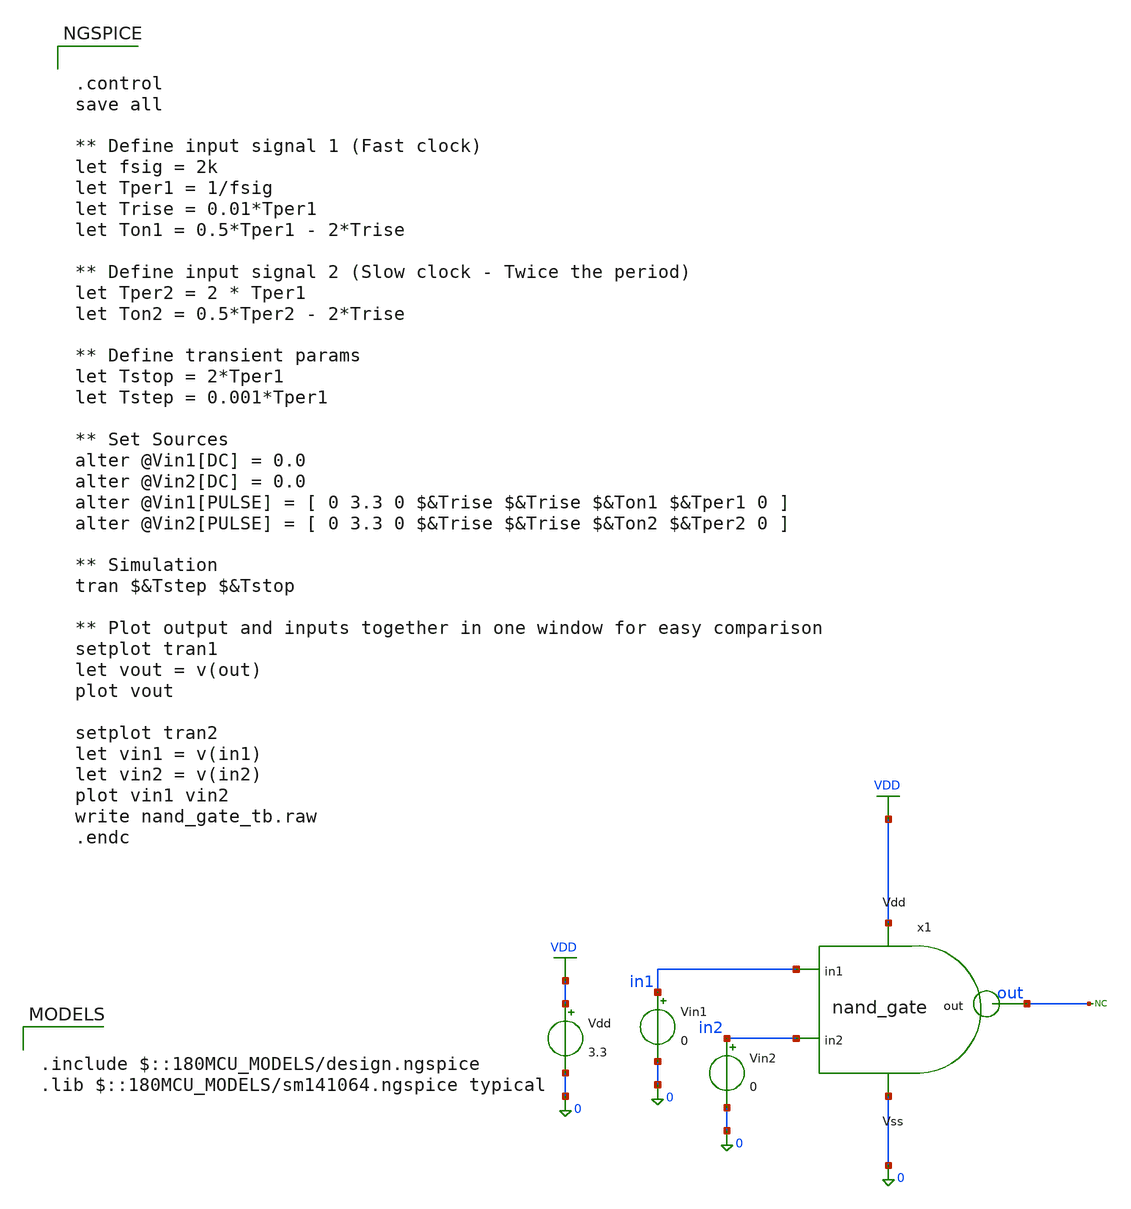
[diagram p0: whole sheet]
** sch_path: NAND/Nand_Gate/xschem/nand_gate_tb.sch
**.subckt nand_gate_tb
Vdd VDD 0 3.3
Vin1 in1 0 0
* noconn out
x1 VDD in1 out in2 0 nand_gate
Vin2 in2 0 0
**** begin user architecture code

.include $::180MCU_MODELS/design.ngspice
.lib $::180MCU_MODELS/sm141064.ngspice typical



.control
save all

** Define input signal 1 (Fast clock)
let fsig = 2k
let Tper1 = 1/fsig
let Trise = 0.01*Tper1
let Ton1 = 0.5*Tper1 - 2*Trise

** Define input signal 2 (Slow clock - Twice the period)
let Tper2 = 2 * Tper1
let Ton2 = 0.5*Tper2 - 2*Trise

** Define transient params
let Tstop = 2*Tper1
let Tstep = 0.001*Tper1

** Set Sources
alter @Vin1[DC] = 0.0
alter @Vin2[DC] = 0.0
alter @Vin1[PULSE] = [ 0 3.3 0 $&Trise $&Trise $&Ton1 $&Tper1 0 ]
alter @Vin2[PULSE] = [ 0 3.3 0 $&Trise $&Trise $&Ton2 $&Tper2 0 ]

** Simulation
tran $&Tstep $&Tstop

** Plot output and inputs together in one window for easy comparison
setplot tran1
let vout = v(out)
plot vout

setplot tran2
let vin1 = v(in1)
let vin2 = v(in2)
plot vin1 vin2
write nand_gate_tb.raw
.endc


**** end user architecture code
**.ends

* expanding   symbol:  APIC/NAND_Gate/nand_gate.sym # of pins=5
** sym_path: NAND/Nand_Gate/xschem/nand_gate.sym
** sch_path: NAND/Nand_Gate/xschem/nand_gate.sch
.subckt nand_gate Vdd in1 out in2 Vss
*.ipin in1
*.opin out
*.ipin Vdd
*.ipin Vss
*.ipin in2
XM3 out in2 Vdd Vdd pfet_03v3 L=0.28u W=2.00u nf=1 ad='int((nf+1)/2) * W/nf * 0.18u' as='int((nf+2)/2) * W/nf * 0.18u'
+ pd='2*int((nf+1)/2) * (W/nf + 0.18u)' ps='2*int((nf+2)/2) * (W/nf + 0.18u)' nrd='0.18u / W' nrs='0.18u / W'
+ sa=0 sb=0 sd=0 m=1
XM1 out in1 net1 Vss nfet_03v3 L=1.00u W=0.42u nf=1 ad='int((nf+1)/2) * W/nf * 0.18u' as='int((nf+2)/2) * W/nf * 0.18u'
+ pd='2*int((nf+1)/2) * (W/nf + 0.18u)' ps='2*int((nf+2)/2) * (W/nf + 0.18u)' nrd='0.18u / W' nrs='0.18u / W'
+ sa=0 sb=0 sd=0 m=1
XM2 out in1 Vdd Vdd pfet_03v3 L=0.28u W=2.00u nf=1 ad='int((nf+1)/2) * W/nf * 0.18u' as='int((nf+2)/2) * W/nf * 0.18u'
+ pd='2*int((nf+1)/2) * (W/nf + 0.18u)' ps='2*int((nf+2)/2) * (W/nf + 0.18u)' nrd='0.18u / W' nrs='0.18u / W'
+ sa=0 sb=0 sd=0 m=1
XM4 net1 in2 Vss Vss nfet_03v3 L=1.00u W=0.42u nf=1 ad='int((nf+1)/2) * W/nf * 0.18u' as='int((nf+2)/2) * W/nf * 0.18u'
+ pd='2*int((nf+1)/2) * (W/nf + 0.18u)' ps='2*int((nf+2)/2) * (W/nf + 0.18u)' nrd='0.18u / W' nrs='0.18u / W'
+ sa=0 sb=0 sd=0 m=1
.ends

.GLOBAL VDD
.end
